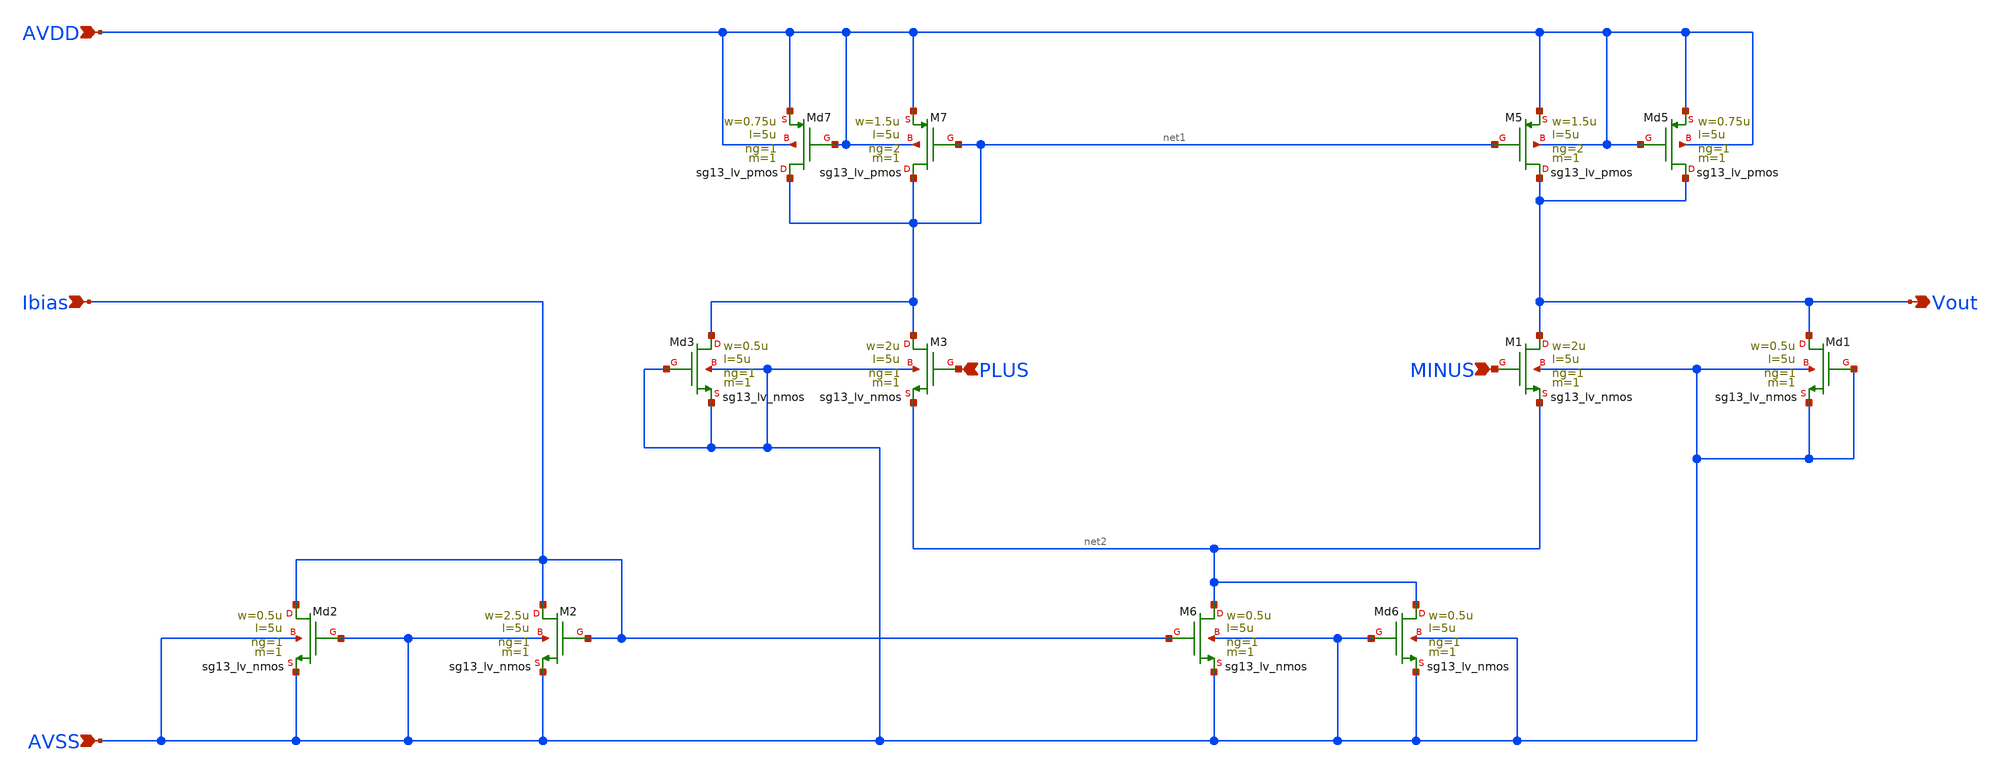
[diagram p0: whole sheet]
** sch_path: Designs/otas/1_schematics/5tota.sch
* (c) 2025 Thesis_HP, Apache-2.0 license
**.subckt 5tota PLUS AVDD Ibias AVSS MINUS Vout
*.ipin PLUS
*.ipin AVDD
*.ipin Ibias
*.ipin AVSS
*.ipin MINUS
*.opin Vout
XM3 net1 PLUS net2 AVSS sg13_lv_nmos w=2u l=5u ng=1 m=1 mm_ok=1
XM5 Vout net1 AVDD AVDD sg13_lv_pmos w=1.5u l=5u ng=2 m=1 mm_ok=1
XM7 net1 net1 AVDD AVDD sg13_lv_pmos w=1.5u l=5u ng=2 m=1 mm_ok=1
XMd3 net1 AVSS AVSS AVSS sg13_lv_nmos w=0.5u l=5u ng=1 m=1 mm_ok=1
XMd5 Vout AVDD AVDD AVDD sg13_lv_pmos w=0.75u l=5u ng=1 m=1 mm_ok=1
XMd7 net1 AVDD AVDD AVDD sg13_lv_pmos w=0.75u l=5u ng=1 m=1 mm_ok=1
XM6 net2 Ibias AVSS AVSS sg13_lv_nmos w=0.5u l=5u ng=1 m=1 mm_ok=1
XM2 Ibias Ibias AVSS AVSS sg13_lv_nmos w=2.5u l=5u ng=1 m=1 mm_ok=1
XMd6 net2 AVSS AVSS AVSS sg13_lv_nmos w=0.5u l=5u ng=1 m=1 mm_ok=1
XM1 Vout MINUS net2 AVSS sg13_lv_nmos w=2u l=5u ng=1 m=1 mm_ok=1
XMd1 Vout AVSS AVSS AVSS sg13_lv_nmos w=0.5u l=5u ng=1 m=1 mm_ok=1
XMd2 Ibias AVSS AVSS AVSS sg13_lv_nmos w=0.5u l=5u ng=1 m=1 mm_ok=1
**.ends
.end
